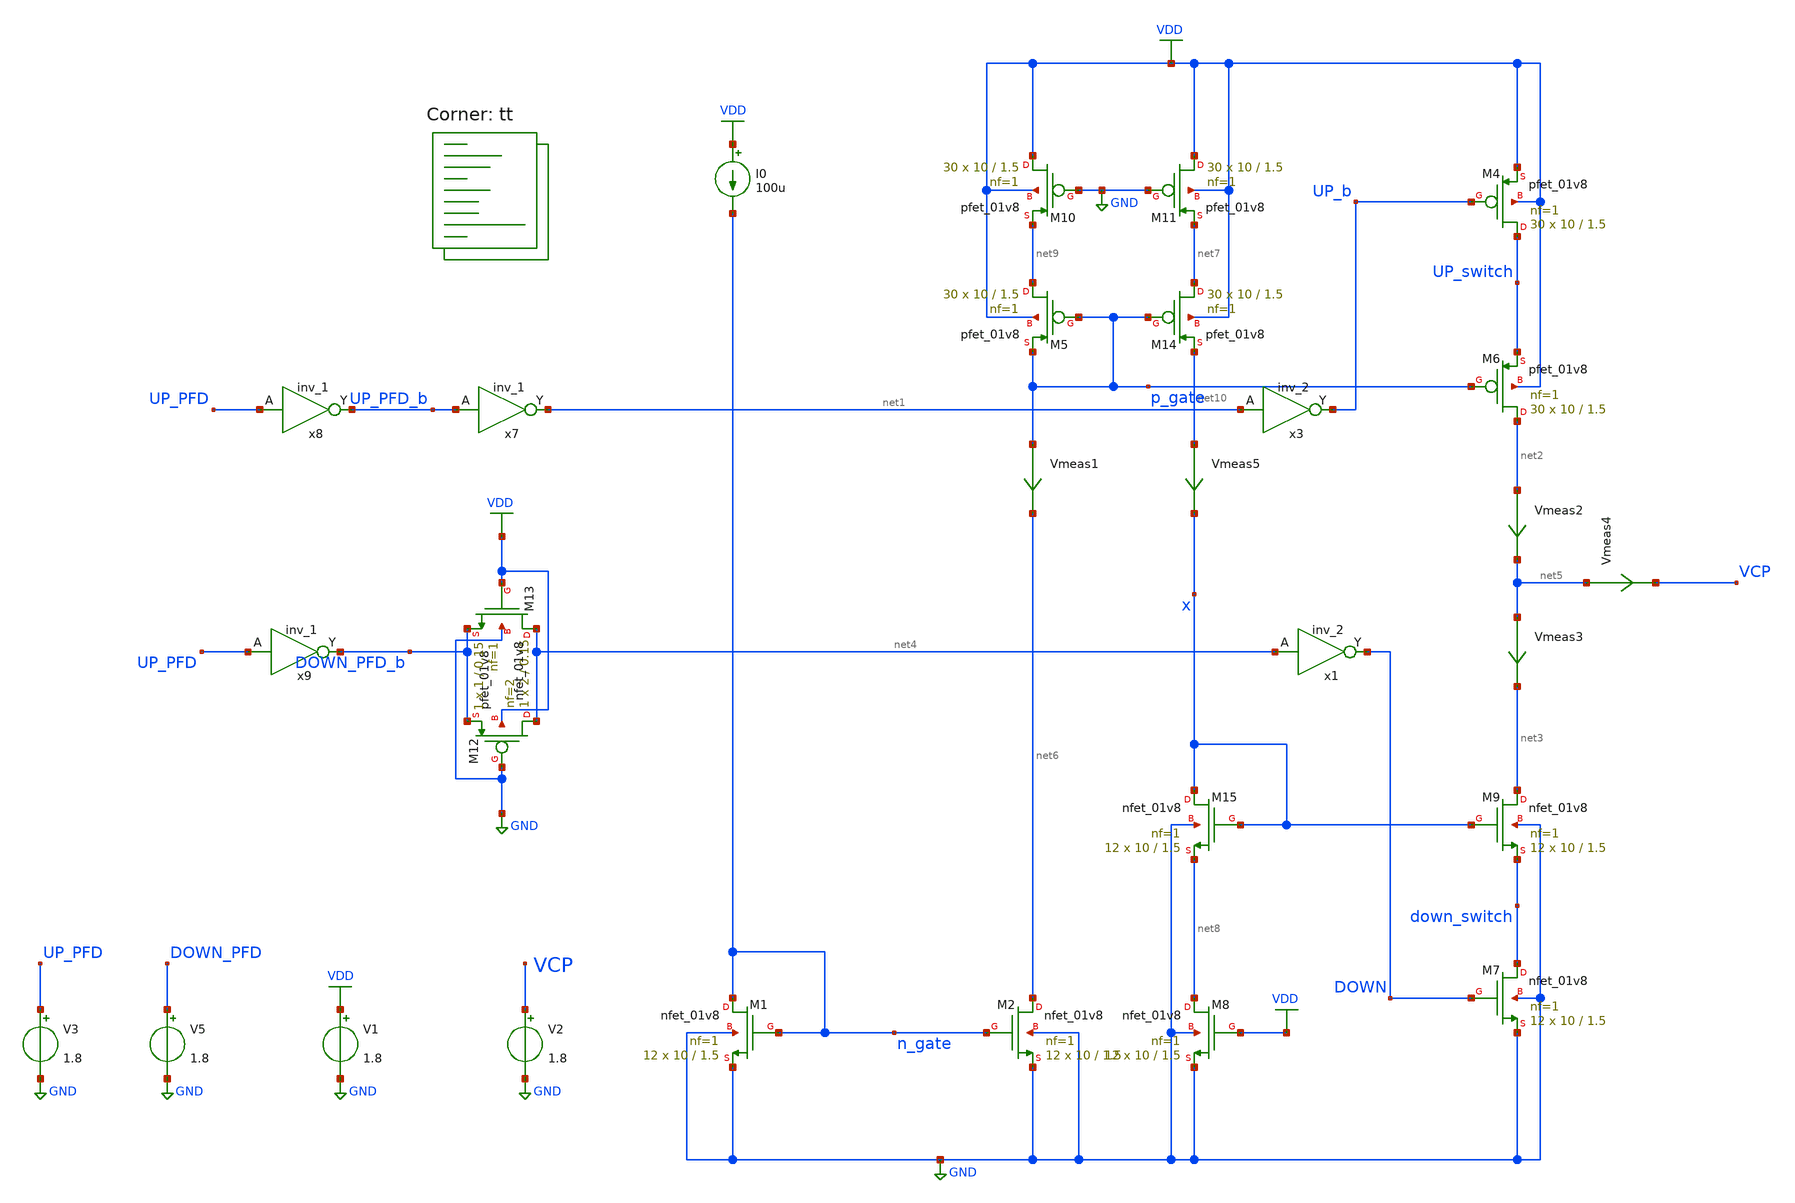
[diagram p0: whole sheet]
** sch_path: projects/pll/charge_pump/xschem_ngspice/charge_pump_DC.sch
**.subckt charge_pump_DC
XM1 n_gate n_gate GND GND sky130_fd_pr__nfet_01v8 L=1.5 W=10 nf=1 ad='int((nf+1)/2) * W/nf * 0.29' as='int((nf+2)/2) * W/nf * 0.29'
+ pd='2*int((nf+1)/2) * (W/nf + 0.29)' ps='2*int((nf+2)/2) * (W/nf + 0.29)' nrd='0.29 / W' nrs='0.29 / W'
+ sa=0 sb=0 sd=0 mult=12 m=12
XM2 net6 n_gate GND GND sky130_fd_pr__nfet_01v8 L=1.5 W=10 nf=1 ad='int((nf+1)/2) * W/nf * 0.29' as='int((nf+2)/2) * W/nf * 0.29'
+ pd='2*int((nf+1)/2) * (W/nf + 0.29)' ps='2*int((nf+2)/2) * (W/nf + 0.29)' nrd='0.29 / W' nrs='0.29 / W'
+ sa=0 sb=0 sd=0 mult=12 m=12
V1 VDD GND 1.8
I0 VDD n_gate 100u
Vmeas1 p_gate net6 0
.save i(vmeas1)
XM6 net2 p_gate UP_switch VDD sky130_fd_pr__pfet_01v8 L=1.5 W=10 nf=1 ad='int((nf+1)/2) * W/nf * 0.29'
+ as='int((nf+2)/2) * W/nf * 0.29' pd='2*int((nf+1)/2) * (W/nf + 0.29)' ps='2*int((nf+2)/2) * (W/nf + 0.29)'
+ nrd='0.29 / W' nrs='0.29 / W' sa=0 sb=0 sd=0 mult=30 m=30
Vmeas2 net2 net5 0
.save i(vmeas2)
Vmeas3 net5 net3 0
.save i(vmeas3)
XM9 net3 x down_switch GND sky130_fd_pr__nfet_01v8 L=1.5 W=10 nf=1 ad='int((nf+1)/2) * W/nf * 0.29' as='int((nf+2)/2) * W/nf * 0.29'
+ pd='2*int((nf+1)/2) * (W/nf + 0.29)' ps='2*int((nf+2)/2) * (W/nf + 0.29)' nrd='0.29 / W' nrs='0.29 / W'
+ sa=0 sb=0 sd=0 mult=12 m=12
XM12 net4 GND DOWN_PFD_b VDD sky130_fd_pr__pfet_01v8 L=0.15 W=2 nf=2 ad='int((nf+1)/2) * W/nf * 0.29'
+ as='int((nf+2)/2) * W/nf * 0.29' pd='2*int((nf+1)/2) * (W/nf + 0.29)' ps='2*int((nf+2)/2) * (W/nf + 0.29)'
+ nrd='0.29 / W' nrs='0.29 / W' sa=0 sb=0 sd=0 mult=1 m=1
XM13 net4 VDD DOWN_PFD_b GND sky130_fd_pr__nfet_01v8 L=0.15 W=1 nf=1 ad='int((nf+1)/2) * W/nf * 0.29'
+ as='int((nf+2)/2) * W/nf * 0.29' pd='2*int((nf+1)/2) * (W/nf + 0.29)' ps='2*int((nf+2)/2) * (W/nf + 0.29)'
+ nrd='0.29 / W' nrs='0.29 / W' sa=0 sb=0 sd=0 mult=1 m=1
x7 UP_PFD_b GND GND VDD VDD net1 sky130_fd_sc_hd__inv_1
x8 UP_PFD GND GND VDD VDD UP_PFD_b sky130_fd_sc_hd__inv_1
x9 UP_PFD GND GND VDD VDD DOWN_PFD_b sky130_fd_sc_hd__inv_1
x3 net1 GND GND VDD VDD UP_b sky130_fd_sc_hd__inv_2
x1 net4 GND GND VDD VDD DOWN sky130_fd_sc_hd__inv_2
V3 UP_PFD GND 1.8
V5 DOWN_PFD GND 1.8
XM4 UP_switch UP_b VDD VDD sky130_fd_pr__pfet_01v8 L=1.5 W=10 nf=1 ad='int((nf+1)/2) * W/nf * 0.29' as='int((nf+2)/2) * W/nf * 0.29'
+ pd='2*int((nf+1)/2) * (W/nf + 0.29)' ps='2*int((nf+2)/2) * (W/nf + 0.29)' nrd='0.29 / W' nrs='0.29 / W'
+ sa=0 sb=0 sd=0 mult=30 m=30
XM5 net9 p_gate p_gate VDD sky130_fd_pr__pfet_01v8 L=1.5 W=10 nf=1 ad='int((nf+1)/2) * W/nf * 0.29' as='int((nf+2)/2) * W/nf * 0.29'
+ pd='2*int((nf+1)/2) * (W/nf + 0.29)' ps='2*int((nf+2)/2) * (W/nf + 0.29)' nrd='0.29 / W' nrs='0.29 / W'
+ sa=0 sb=0 sd=0 mult=30 m=30
XM10 VDD GND net9 VDD sky130_fd_pr__pfet_01v8 L=1.5 W=10 nf=1 ad='int((nf+1)/2) * W/nf * 0.29' as='int((nf+2)/2) * W/nf * 0.29'
+ pd='2*int((nf+1)/2) * (W/nf + 0.29)' ps='2*int((nf+2)/2) * (W/nf + 0.29)' nrd='0.29 / W' nrs='0.29 / W'
+ sa=0 sb=0 sd=0 mult=30 m=30
XM11 VDD GND net7 VDD sky130_fd_pr__pfet_01v8 L=1.5 W=10 nf=1 ad='int((nf+1)/2) * W/nf * 0.29' as='int((nf+2)/2) * W/nf * 0.29'
+ pd='2*int((nf+1)/2) * (W/nf + 0.29)' ps='2*int((nf+2)/2) * (W/nf + 0.29)' nrd='0.29 / W' nrs='0.29 / W'
+ sa=0 sb=0 sd=0 mult=30 m=30
XM14 net7 p_gate net10 VDD sky130_fd_pr__pfet_01v8 L=1.5 W=10 nf=1 ad='int((nf+1)/2) * W/nf * 0.29' as='int((nf+2)/2) * W/nf * 0.29'
+ pd='2*int((nf+1)/2) * (W/nf + 0.29)' ps='2*int((nf+2)/2) * (W/nf + 0.29)' nrd='0.29 / W' nrs='0.29 / W'
+ sa=0 sb=0 sd=0 mult=30 m=30
XM7 down_switch DOWN GND GND sky130_fd_pr__nfet_01v8 L=1.5 W=10 nf=1 ad='int((nf+1)/2) * W/nf * 0.29'
+ as='int((nf+2)/2) * W/nf * 0.29' pd='2*int((nf+1)/2) * (W/nf + 0.29)' ps='2*int((nf+2)/2) * (W/nf + 0.29)'
+ nrd='0.29 / W' nrs='0.29 / W' sa=0 sb=0 sd=0 mult=12 m=12
XM8 net8 VDD GND GND sky130_fd_pr__nfet_01v8 L=1.5 W=10 nf=1 ad='int((nf+1)/2) * W/nf * 0.29' as='int((nf+2)/2) * W/nf * 0.29'
+ pd='2*int((nf+1)/2) * (W/nf + 0.29)' ps='2*int((nf+2)/2) * (W/nf + 0.29)' nrd='0.29 / W' nrs='0.29 / W'
+ sa=0 sb=0 sd=0 mult=12 m=12
XM15 x x net8 GND sky130_fd_pr__nfet_01v8 L=1.5 W=10 nf=1 ad='int((nf+1)/2) * W/nf * 0.29' as='int((nf+2)/2) * W/nf * 0.29'
+ pd='2*int((nf+1)/2) * (W/nf + 0.29)' ps='2*int((nf+2)/2) * (W/nf + 0.29)' nrd='0.29 / W' nrs='0.29 / W'
+ sa=0 sb=0 sd=0 mult=12 m=12
Vmeas5 net10 x 0
.save i(vmeas5)
V2 VCP GND 1.8
Vmeas4 net5 VCP 0
.save i(vmeas4)
**** begin user architecture code
.lib $::SKYWATER_MODELS/sky130.lib.spice tt



.include /foss/pdks/sky130A/libs.ref/sky130_fd_sc_hd/spice/sky130_fd_sc_hd.spice

.option method=gear trtol1
.option wnflag=1
* .option savecurrents

* .temp = 75

*.ic v(vout) = 1.2

.save  v(up_pfd) v(down_pfd) v(up_pfd_b) v(down_pfd_b) v(up) v(up_b) v(down) v(down_b) v(v2) v(x) v(vcp) v(up_switch) v(down_switch) v(p_gate) v(n_gate) v(x2.p_bias) v(x2.n_bias) v(x2.v_common_p) v(x2.v_common_n) v(x2.p_left) v(x2.p_right) v(x2.n_left) v(x2.n_right) v(f_ref) v(f_vco) v(x4.qa) v(x4.qa_b) v(x4.qb) v(x4.qb_b) v(x4.qa) v(x4.e) v(x4.e_b) v(x4.f) v(x4.f_b) v(x4.before_reset) v(x4.reset)


.control
  * save v(up_pfd) v(down_pfd) v(up_pfd_b) v(down_pfd_b) v(up) v(up_b) v(down) v(down_b) v(x)
+ v(vout) v(up_input) v(down_input)
  * save all

  * tran 1ns 10us
  dc v2 0 1.8 0.01 v3 0 1.8 1.8
  remzerovec
  write charge_pump_DC.raw
  * wrdata /foss/designs/my_design/projects/pll/pfd/xschem_ngspice/charge_pump2_QA.txt v(osc)
  set appendwrite

.endc






**** end user architecture code
**.ends
.GLOBAL VDD
.GLOBAL GND
.end
